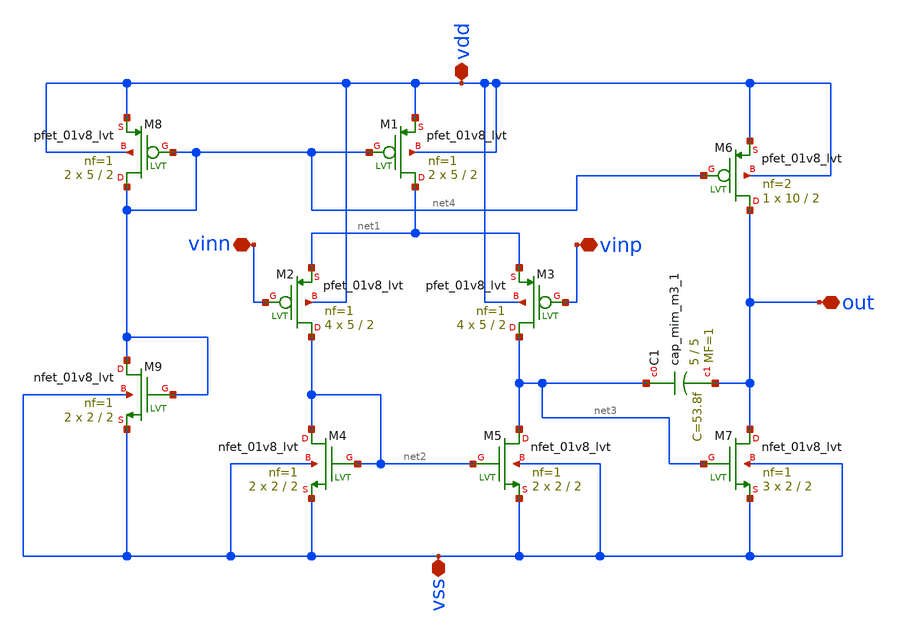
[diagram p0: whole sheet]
** sch_path: ANOTHER_SOLUTIONS_CONSIDERED/ANOTHER_BIAS_FOR_TEMPERATURE_SENSOR/OPAMP/XSCHEM/OPAMP_lvt_PMOS.sch
**.subckt OPAMP_lvt_PMOS vdd vss out vinp vinn
*.iopin vdd
*.iopin vss
*.iopin out
*.iopin vinp
*.iopin vinn
XC1 net3 out sky130_fd_pr__cap_mim_m3_1 W=5 L=5 MF=1 m=1
XM1 net1 net4 vdd vdd sky130_fd_pr__pfet_01v8_lvt L=2 W=5 nf=1 ad='int((nf+1)/2) * W/nf * 0.29' as='int((nf+2)/2) * W/nf * 0.29'
+ pd='2*int((nf+1)/2) * (W/nf + 0.29)' ps='2*int((nf+2)/2) * (W/nf + 0.29)' nrd='0.29 / W' nrs='0.29 / W'
+ sa=0 sb=0 sd=0 mult=2 m=2
XM2 net2 vinn net1 vdd sky130_fd_pr__pfet_01v8_lvt L=2 W=5 nf=1 ad='int((nf+1)/2) * W/nf * 0.29' as='int((nf+2)/2) * W/nf * 0.29'
+ pd='2*int((nf+1)/2) * (W/nf + 0.29)' ps='2*int((nf+2)/2) * (W/nf + 0.29)' nrd='0.29 / W' nrs='0.29 / W'
+ sa=0 sb=0 sd=0 mult=4 m=4
XM3 net3 vinp net1 vdd sky130_fd_pr__pfet_01v8_lvt L=2 W=5 nf=1 ad='int((nf+1)/2) * W/nf * 0.29' as='int((nf+2)/2) * W/nf * 0.29'
+ pd='2*int((nf+1)/2) * (W/nf + 0.29)' ps='2*int((nf+2)/2) * (W/nf + 0.29)' nrd='0.29 / W' nrs='0.29 / W'
+ sa=0 sb=0 sd=0 mult=4 m=4
XM4 net2 net2 vss vss sky130_fd_pr__nfet_01v8_lvt L=2 W=2 nf=1 ad='int((nf+1)/2) * W/nf * 0.29' as='int((nf+2)/2) * W/nf * 0.29'
+ pd='2*int((nf+1)/2) * (W/nf + 0.29)' ps='2*int((nf+2)/2) * (W/nf + 0.29)' nrd='0.29 / W' nrs='0.29 / W'
+ sa=0 sb=0 sd=0 mult=2 m=2
XM5 net3 net2 vss vss sky130_fd_pr__nfet_01v8_lvt L=2 W=2 nf=1 ad='int((nf+1)/2) * W/nf * 0.29' as='int((nf+2)/2) * W/nf * 0.29'
+ pd='2*int((nf+1)/2) * (W/nf + 0.29)' ps='2*int((nf+2)/2) * (W/nf + 0.29)' nrd='0.29 / W' nrs='0.29 / W'
+ sa=0 sb=0 sd=0 mult=2 m=2
XM6 out net4 vdd vdd sky130_fd_pr__pfet_01v8_lvt L=2 W=10 nf=2 ad='int((nf+1)/2) * W/nf * 0.29' as='int((nf+2)/2) * W/nf * 0.29'
+ pd='2*int((nf+1)/2) * (W/nf + 0.29)' ps='2*int((nf+2)/2) * (W/nf + 0.29)' nrd='0.29 / W' nrs='0.29 / W'
+ sa=0 sb=0 sd=0 mult=1 m=1
XM7 out net3 vss vss sky130_fd_pr__nfet_01v8_lvt L=2 W=2 nf=1 ad='int((nf+1)/2) * W/nf * 0.29' as='int((nf+2)/2) * W/nf * 0.29'
+ pd='2*int((nf+1)/2) * (W/nf + 0.29)' ps='2*int((nf+2)/2) * (W/nf + 0.29)' nrd='0.29 / W' nrs='0.29 / W'
+ sa=0 sb=0 sd=0 mult=3 m=3
XM8 net4 net4 vdd vdd sky130_fd_pr__pfet_01v8_lvt L=2 W=5 nf=1 ad='int((nf+1)/2) * W/nf * 0.29' as='int((nf+2)/2) * W/nf * 0.29'
+ pd='2*int((nf+1)/2) * (W/nf + 0.29)' ps='2*int((nf+2)/2) * (W/nf + 0.29)' nrd='0.29 / W' nrs='0.29 / W'
+ sa=0 sb=0 sd=0 mult=2 m=2
XM9 net4 net4 vss vss sky130_fd_pr__nfet_01v8_lvt L=2 W=2 nf=1 ad='int((nf+1)/2) * W/nf * 0.29' as='int((nf+2)/2) * W/nf * 0.29'
+ pd='2*int((nf+1)/2) * (W/nf + 0.29)' ps='2*int((nf+2)/2) * (W/nf + 0.29)' nrd='0.29 / W' nrs='0.29 / W'
+ sa=0 sb=0 sd=0 mult=2 m=2
**.ends
.end
